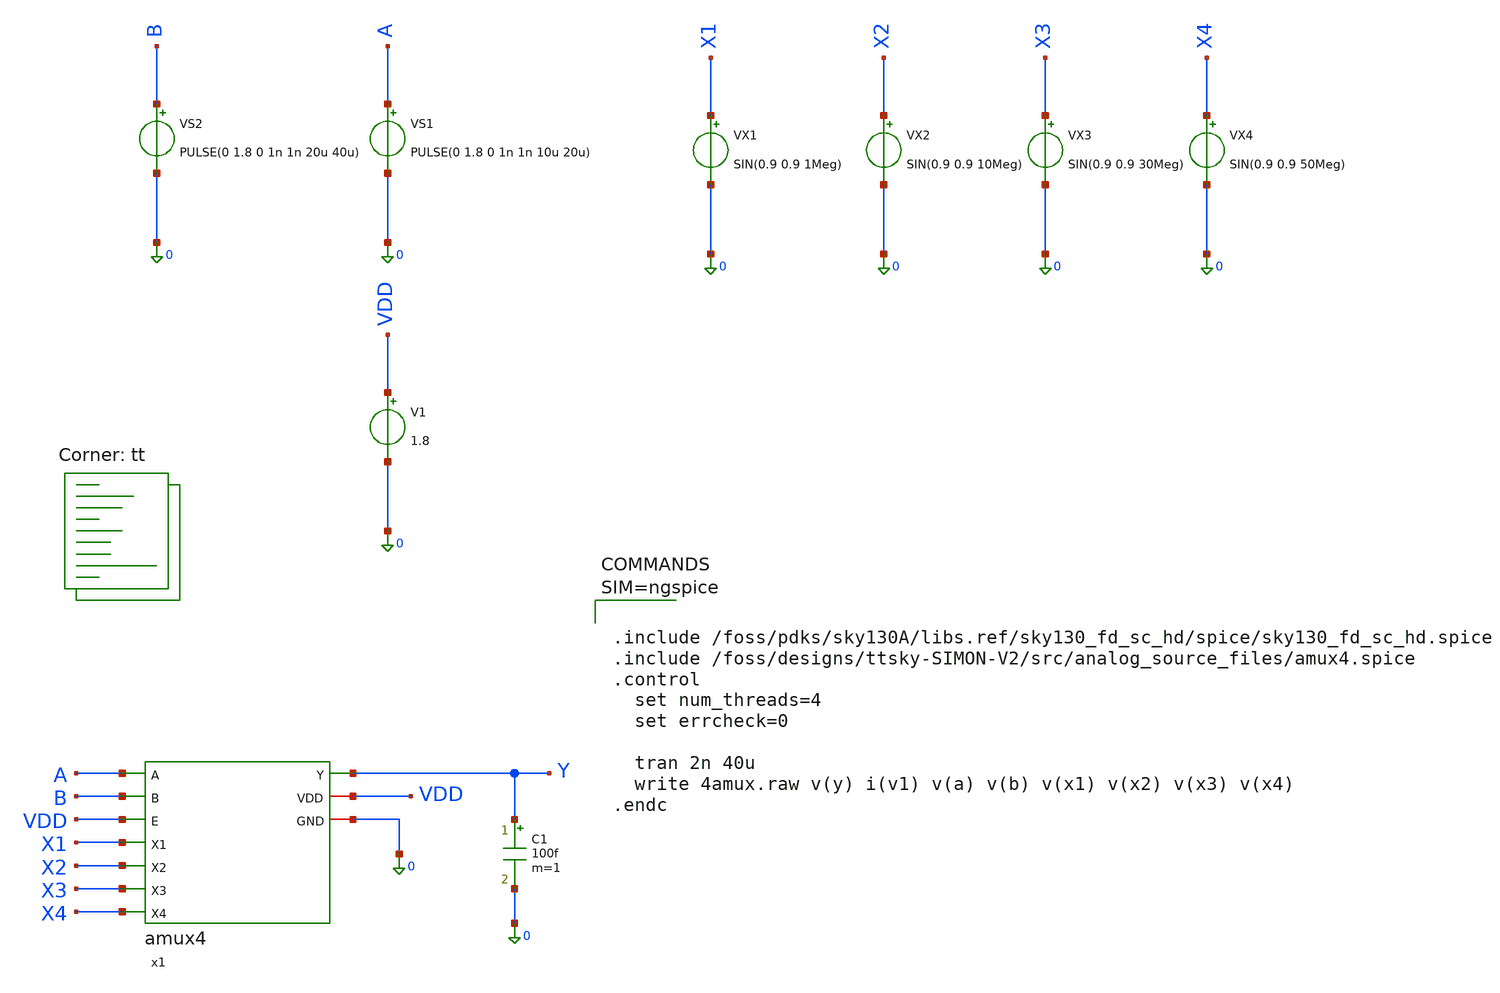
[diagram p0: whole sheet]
** sch_path: src/analog_source_files/amux4_tb.sch
**.subckt amux4_tb
V1 VDD 0 1.8
VS1 A 0 PULSE(0 1.8 0 1n 1n 10u 20u)
VS2 B 0 PULSE(0 1.8 0 1n 1n 20u 40u)
VX1 X1 0 SIN(0.9 0.9 1Meg)
VX2 X2 0 SIN(0.9 0.9 10Meg)
VX3 X3 0 SIN(0.9 0.9 30Meg)
VX4 X4 0 SIN(0.9 0.9 50Meg)
C1 Y 0 100f m=1
x1 X1 A B VDD X2 Y X3 VDD 0 X4 amux4
**** begin user architecture code



.include /foss/pdks/sky130A/libs.ref/sky130_fd_sc_hd/spice/sky130_fd_sc_hd.spice
.include /foss/designs/ttsky-SIMON-V2/src/analog_source_files/amux4.spice
.control
  set num_threads=4
  set errcheck=0

  tran 2n 40u
  write 4amux.raw v(y) i(v1) v(a) v(b) v(x1) v(x2) v(x3) v(x4)
.endc



.lib $::SKYWATER_MODELS/sky130.lib.spice tt
**** end user architecture code
**.ends
.end
